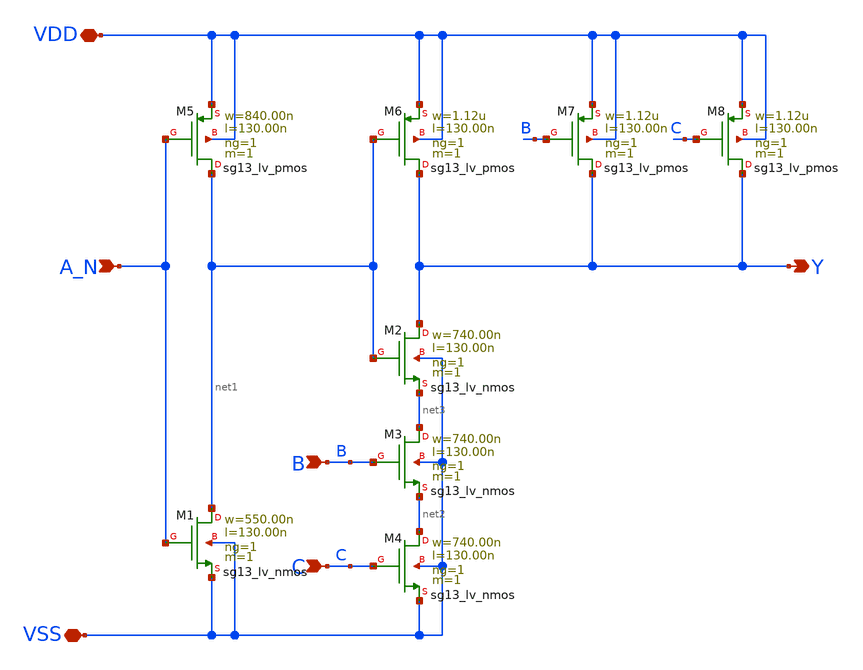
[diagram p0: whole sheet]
** sch_path: ihp-sg13g2/libs.tech/xschem/sg13g2_stdcells/sg13g2_nand3b_1.sch
* Copyright 2023 IHP PDK Authors
* Licensed under the Apache License, Version 2.0 (the "License");
* you may not use this file except in compliance with the License.
* You may obtain a copy of the License at
* https://www.apache.org/licenses/LICENSE-2.0
* Unless required by applicable law or agreed to in writing, software
* distributed under the License is distributed on an "AS IS" BASIS,
* WITHOUT WARRANTIES OR CONDITIONS OF ANY KIND, either express or implied.
* See the License for the specific language governing permissions and
* limitations under the License.
**.subckt sg13g2_nand3b_1 A_N B C Y VDD VSS
*.ipin A_N
*.ipin B
*.ipin C
*.opin Y
*.iopin VDD
*.iopin VSS
XM1 net1 A_N VSS VSS sg13_lv_nmos w=550.00n l=130.00n ng=1 m=1 mm_ok=1
XM2 Y net1 net3 VSS sg13_lv_nmos w=740.00n l=130.00n ng=1 m=1 mm_ok=1
XM3 net3 B net2 VSS sg13_lv_nmos w=740.00n l=130.00n ng=1 m=1 mm_ok=1
XM4 net2 C VSS VSS sg13_lv_nmos w=740.00n l=130.00n ng=1 m=1 mm_ok=1
XM5 net1 A_N VDD VDD sg13_lv_pmos w=840.00n l=130.00n ng=1 m=1 mm_ok=1
XM6 Y net1 VDD VDD sg13_lv_pmos w=1.12u l=130.00n ng=1 m=1 mm_ok=1
XM7 Y B VDD VDD sg13_lv_pmos w=1.12u l=130.00n ng=1 m=1 mm_ok=1
XM8 Y C VDD VDD sg13_lv_pmos w=1.12u l=130.00n ng=1 m=1 mm_ok=1
**.ends
.end
